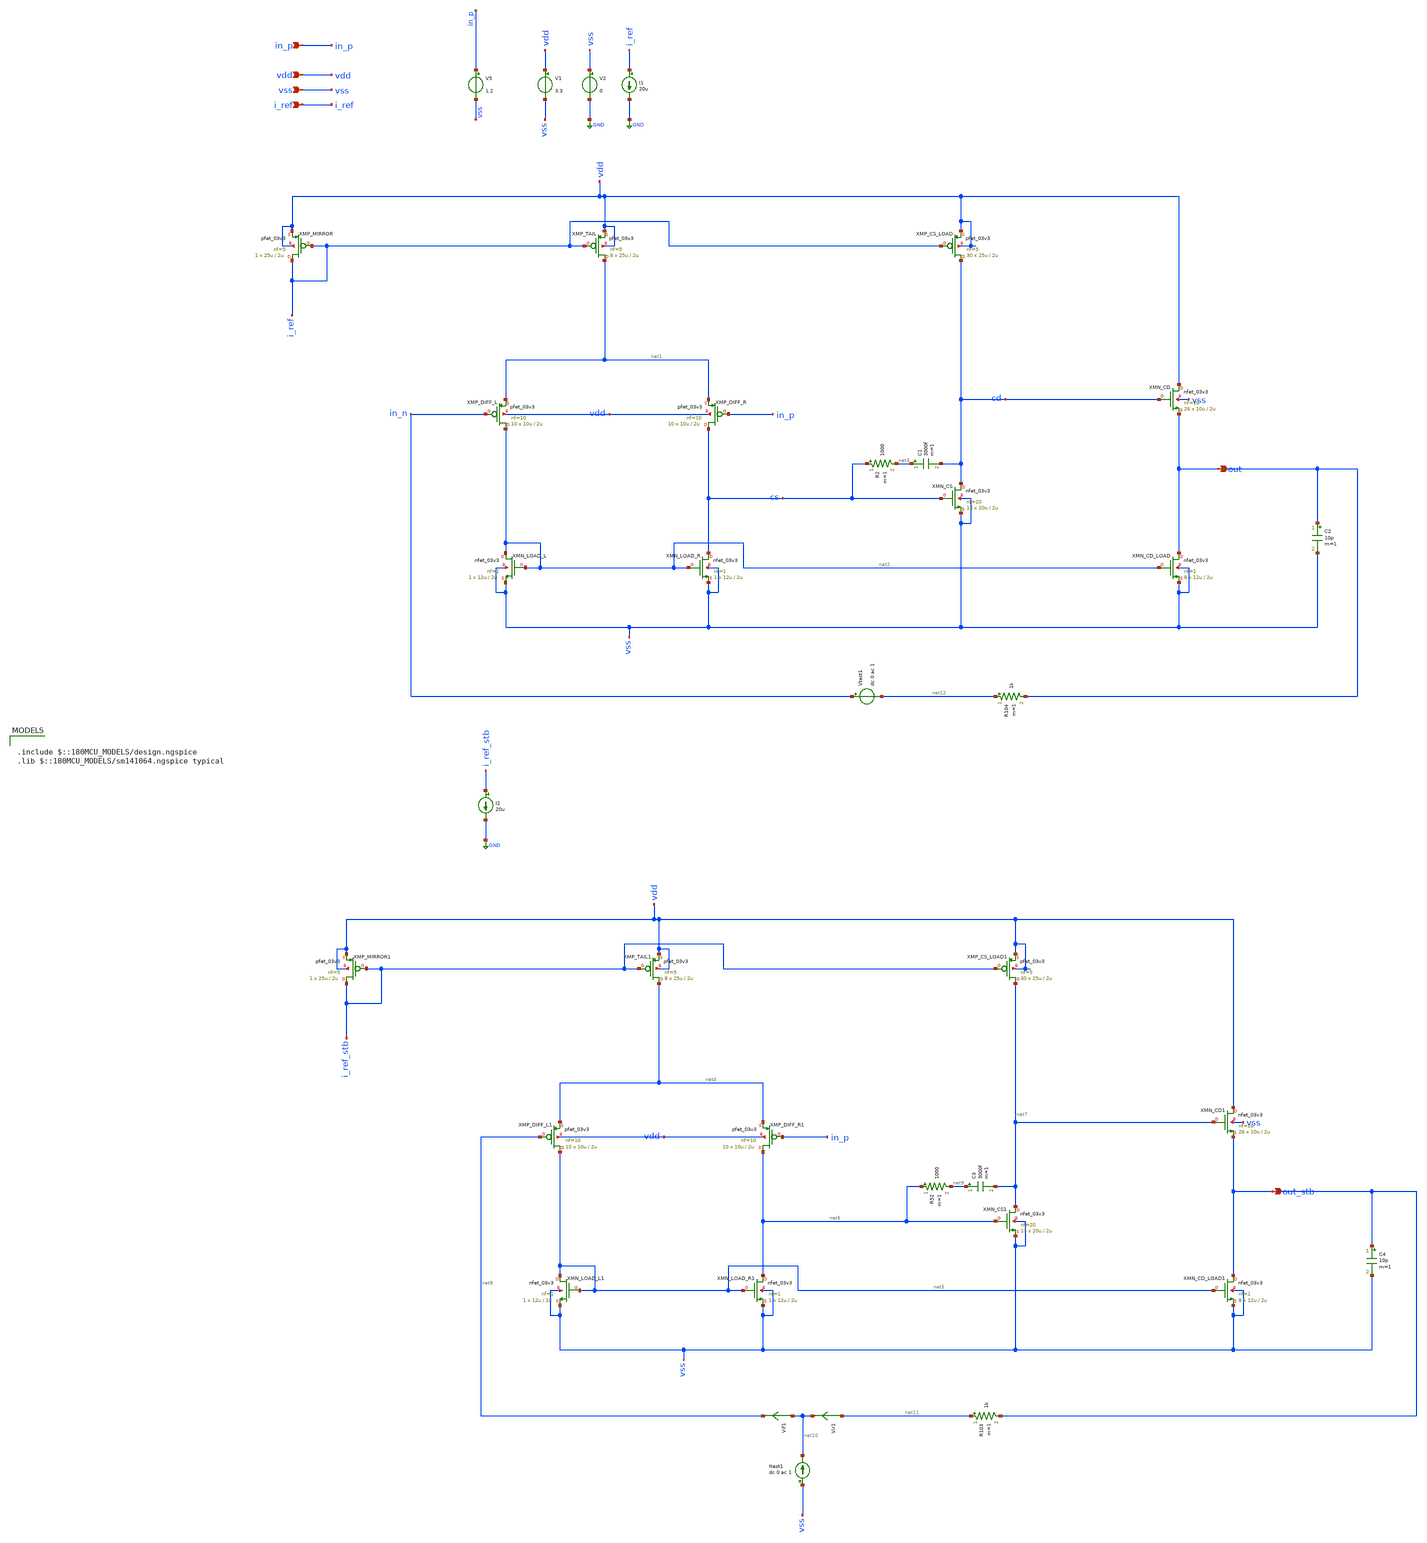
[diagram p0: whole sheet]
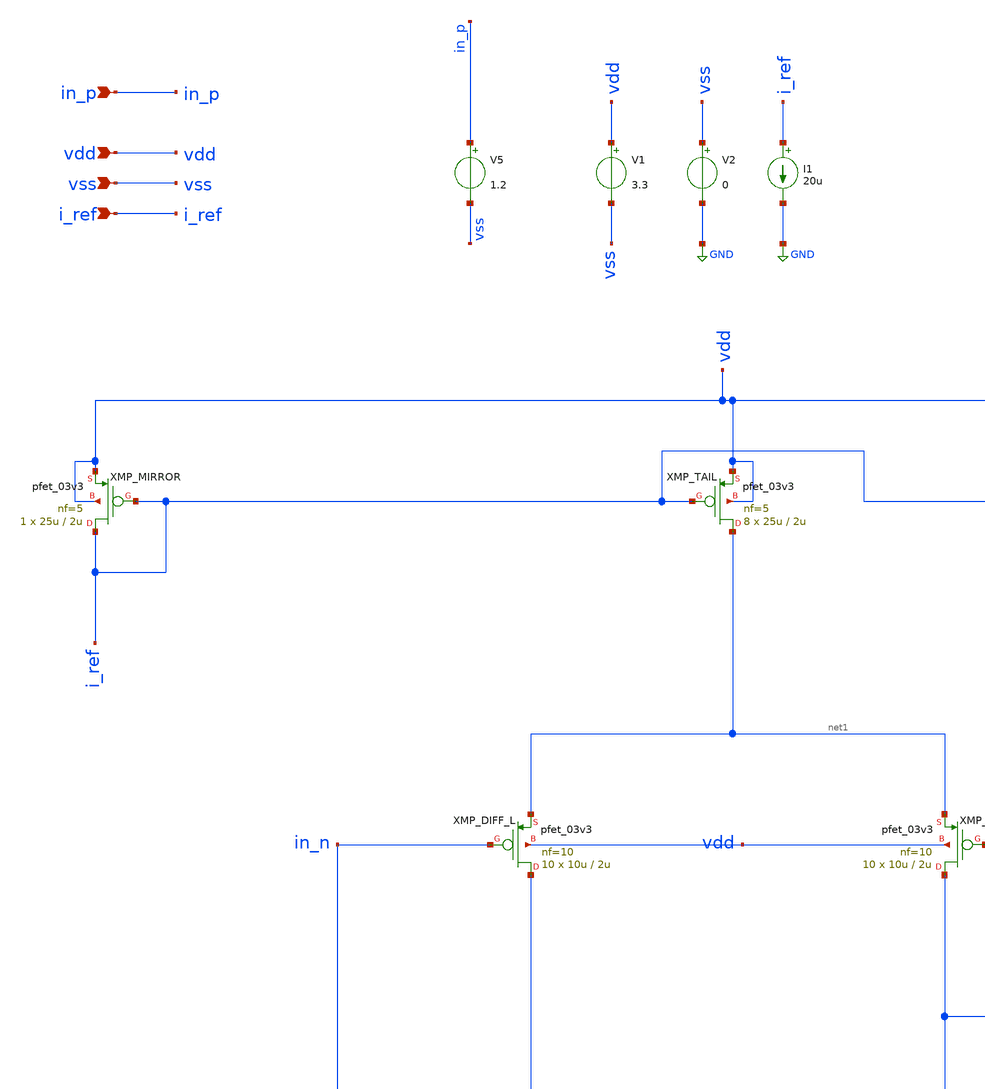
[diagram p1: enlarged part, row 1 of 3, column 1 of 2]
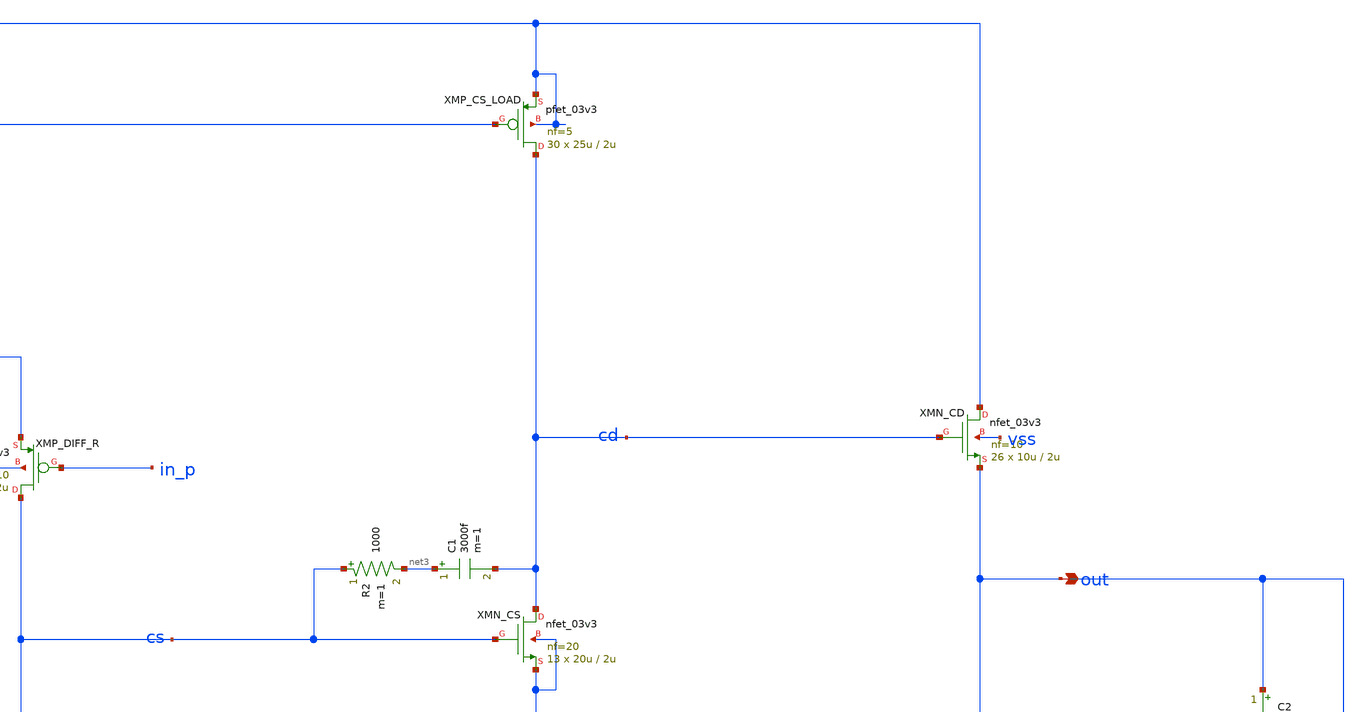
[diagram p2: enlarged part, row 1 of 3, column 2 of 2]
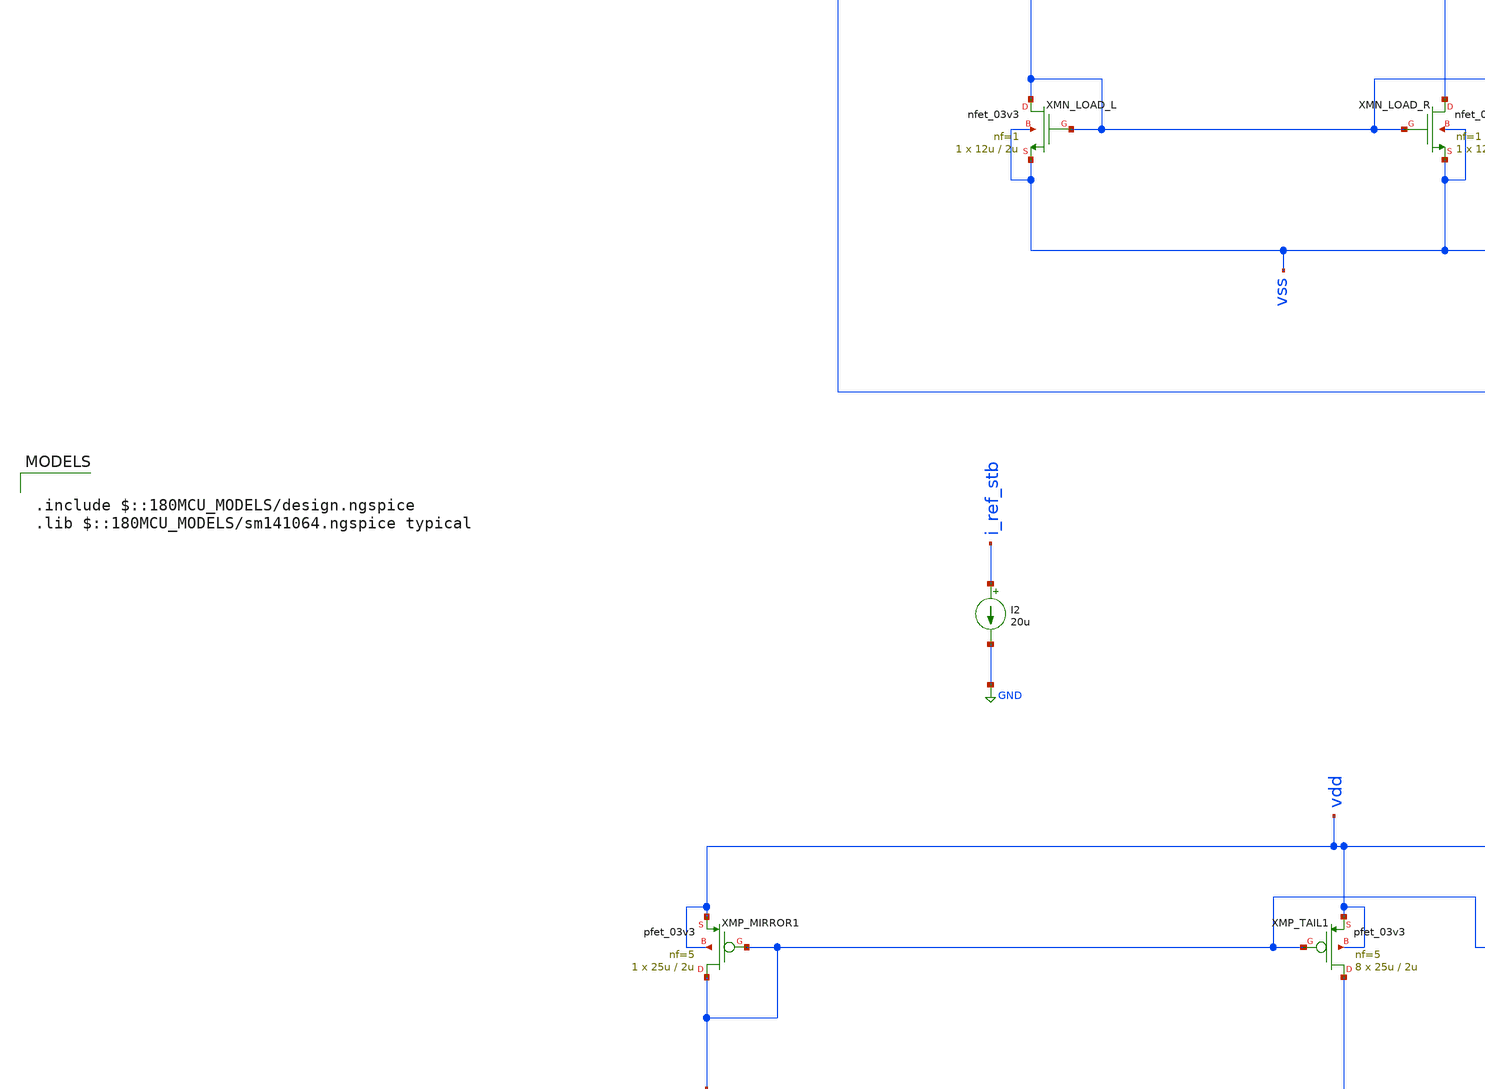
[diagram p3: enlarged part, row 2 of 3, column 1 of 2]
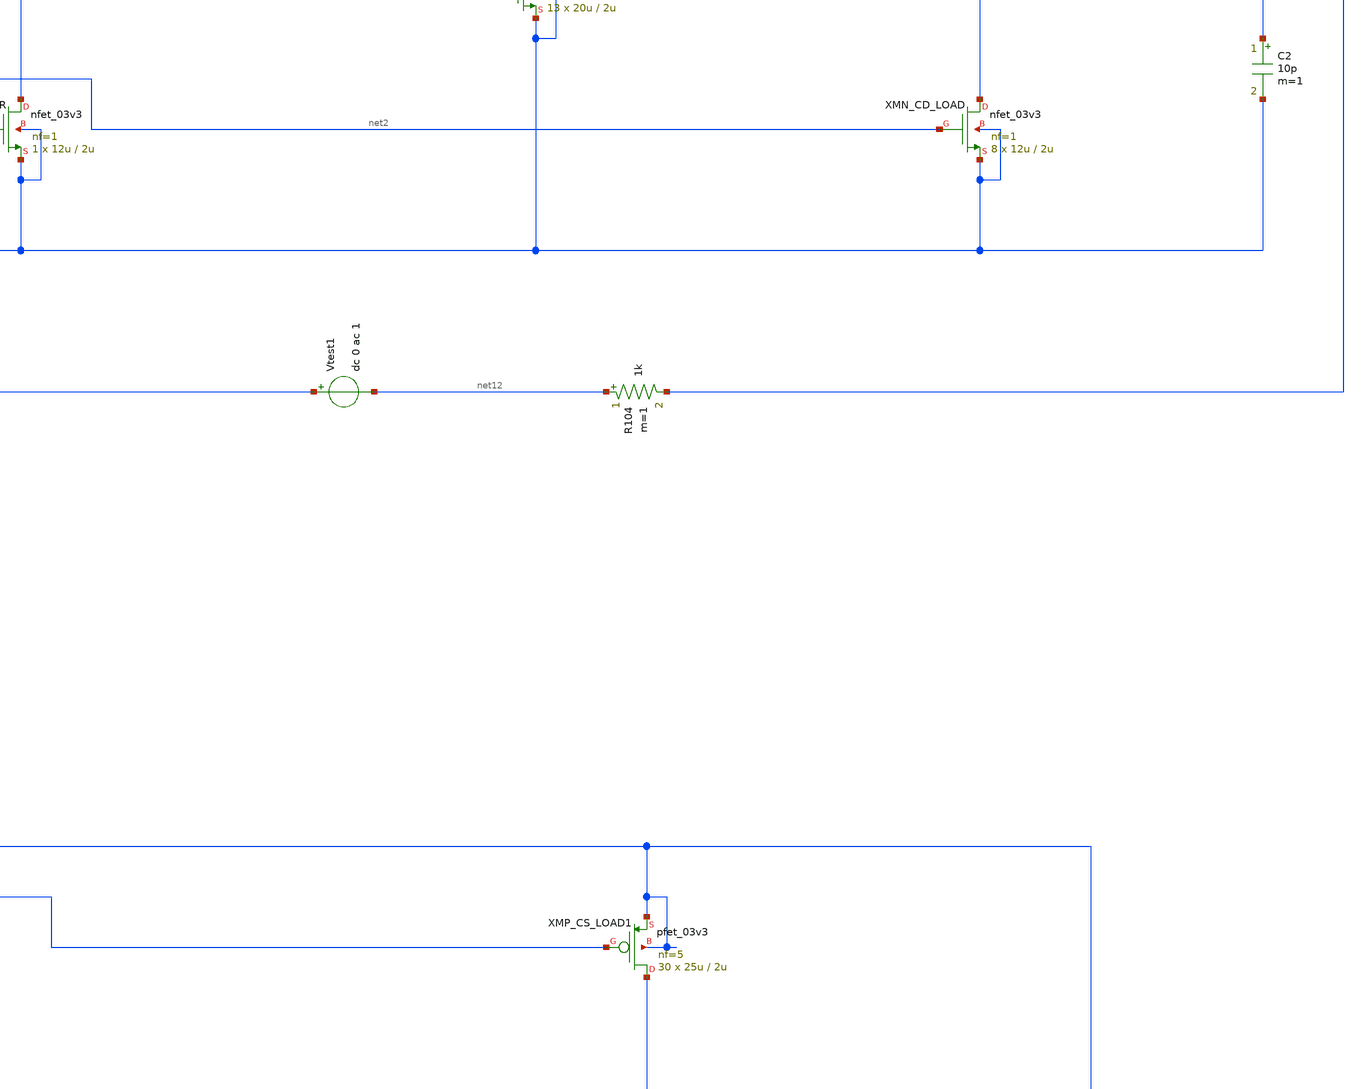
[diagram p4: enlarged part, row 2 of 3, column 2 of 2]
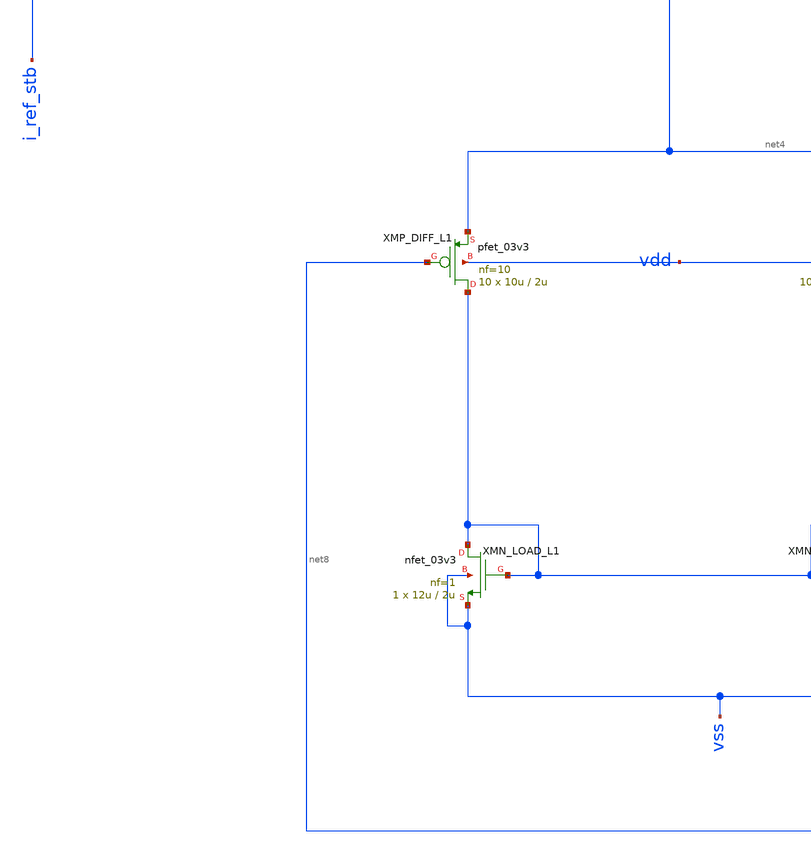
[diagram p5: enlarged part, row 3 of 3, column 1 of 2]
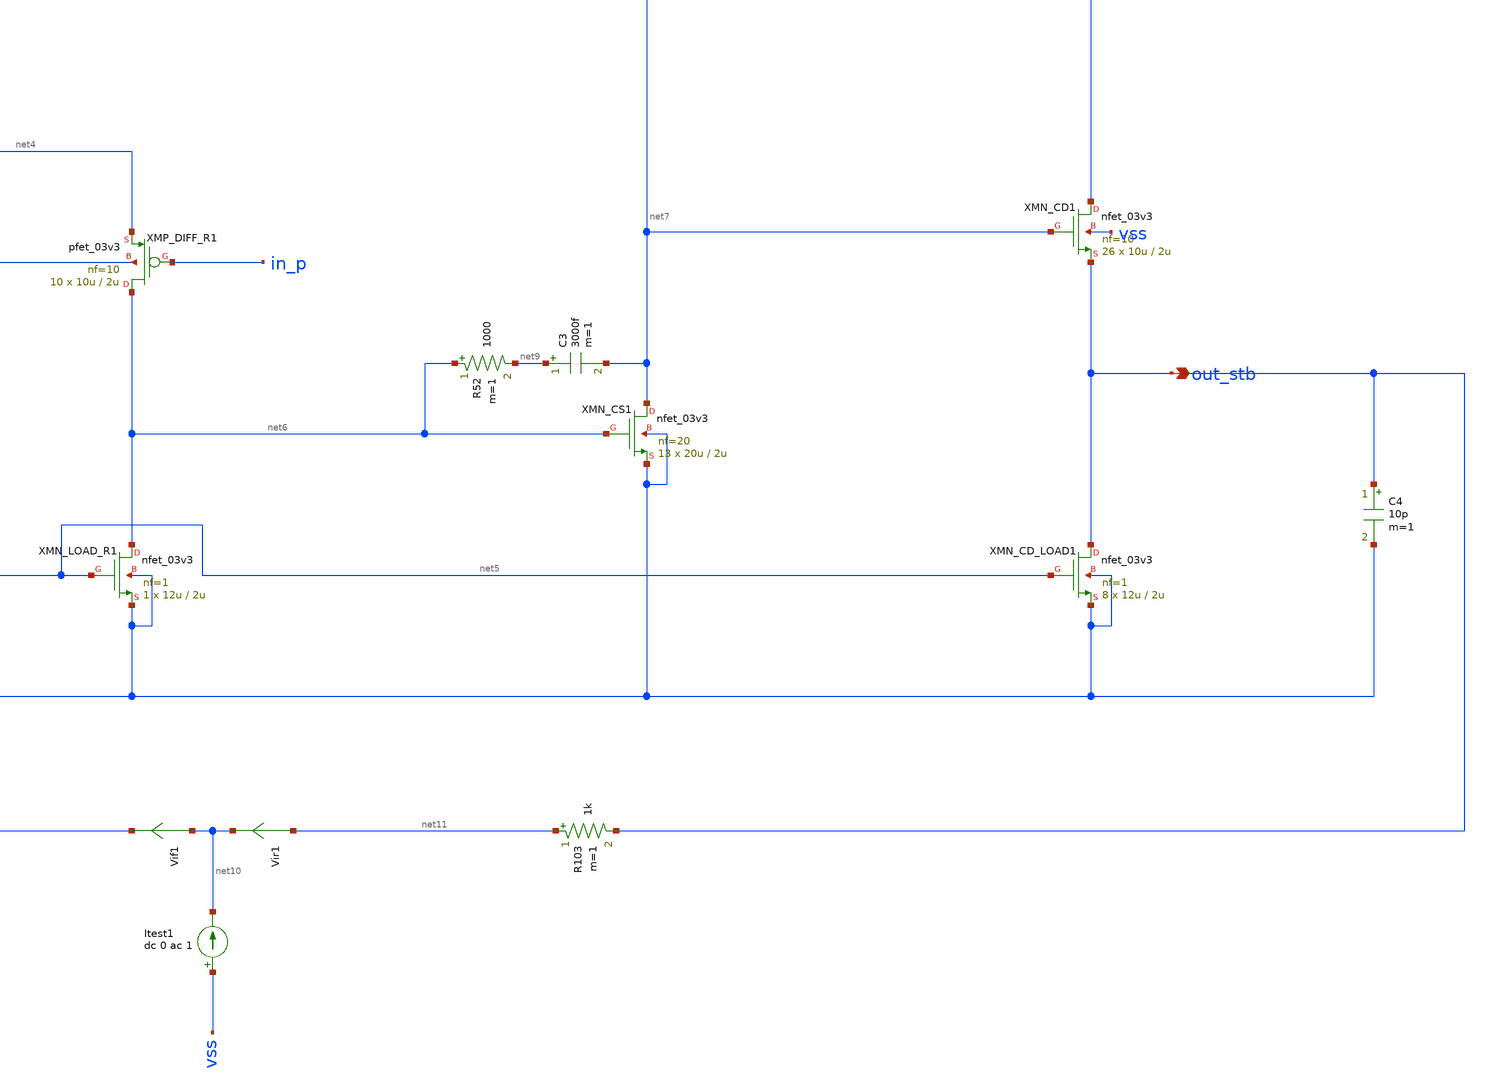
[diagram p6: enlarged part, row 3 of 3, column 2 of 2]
** sch_path: designs/libs/TIA/TIA_TB_stb.sch
**.subckt TIA_TB_stb in_p vdd vss i_ref out out_stb
*.ipin in_p
*.ipin vdd
*.ipin vss
*.ipin i_ref
*.opin out
*.opin out_stb
XMP_TAIL net1 i_ref vdd vdd pfet_03v3 L=2u W=25u nf=5 ad='int((nf+1)/2) * W/nf * 0.18u' as='int((nf+2)/2) * W/nf * 0.18u'
+ pd='2*int((nf+1)/2) * (W/nf + 0.18u)' ps='2*int((nf+2)/2) * (W/nf + 0.18u)' nrd='0.18u / W' nrs='0.18u / W'
+ sa=0 sb=0 sd=0 m=8
XMP_DIFF_L net2 in_n net1 vdd pfet_03v3 L=2u W=10u nf=10 ad='int((nf+1)/2) * W/nf * 0.18u' as='int((nf+2)/2) * W/nf * 0.18u'
+ pd='2*int((nf+1)/2) * (W/nf + 0.18u)' ps='2*int((nf+2)/2) * (W/nf + 0.18u)' nrd='0.18u / W' nrs='0.18u / W'
+ sa=0 sb=0 sd=0 m=10
XMP_DIFF_R cs in_p net1 vdd pfet_03v3 L=2u W=10u nf=10 ad='int((nf+1)/2) * W/nf * 0.18u' as='int((nf+2)/2) * W/nf * 0.18u'
+ pd='2*int((nf+1)/2) * (W/nf + 0.18u)' ps='2*int((nf+2)/2) * (W/nf + 0.18u)' nrd='0.18u / W' nrs='0.18u / W'
+ sa=0 sb=0 sd=0 m=10
XMP_CS_LOAD cd i_ref vdd vdd pfet_03v3 L=2u W=25u nf=5 ad='int((nf+1)/2) * W/nf * 0.18u' as='int((nf+2)/2) * W/nf * 0.18u'
+ pd='2*int((nf+1)/2) * (W/nf + 0.18u)' ps='2*int((nf+2)/2) * (W/nf + 0.18u)' nrd='0.18u / W' nrs='0.18u / W'
+ sa=0 sb=0 sd=0 m=30
XMP_MIRROR i_ref i_ref vdd vdd pfet_03v3 L=2u W=25u nf=5 ad='int((nf+1)/2) * W/nf * 0.18u' as='int((nf+2)/2) * W/nf * 0.18u'
+ pd='2*int((nf+1)/2) * (W/nf + 0.18u)' ps='2*int((nf+2)/2) * (W/nf + 0.18u)' nrd='0.18u / W' nrs='0.18u / W'
+ sa=0 sb=0 sd=0 m=1
XMN_LOAD_R cs net2 vss vss nfet_03v3 L=2u W=12u nf=1 ad='int((nf+1)/2) * W/nf * 0.18u' as='int((nf+2)/2) * W/nf * 0.18u'
+ pd='2*int((nf+1)/2) * (W/nf + 0.18u)' ps='2*int((nf+2)/2) * (W/nf + 0.18u)' nrd='0.18u / W' nrs='0.18u / W'
+ sa=0 sb=0 sd=0 m=1
XMN_LOAD_L net2 net2 vss vss nfet_03v3 L=2u W=12u nf=1 ad='int((nf+1)/2) * W/nf * 0.18u' as='int((nf+2)/2) * W/nf * 0.18u'
+ pd='2*int((nf+1)/2) * (W/nf + 0.18u)' ps='2*int((nf+2)/2) * (W/nf + 0.18u)' nrd='0.18u / W' nrs='0.18u / W'
+ sa=0 sb=0 sd=0 m=1
XMN_CS cd cs vss vss nfet_03v3 L=2u W=20u nf=20 ad='int((nf+1)/2) * W/nf * 0.18u' as='int((nf+2)/2) * W/nf * 0.18u'
+ pd='2*int((nf+1)/2) * (W/nf + 0.18u)' ps='2*int((nf+2)/2) * (W/nf + 0.18u)' nrd='0.18u / W' nrs='0.18u / W'
+ sa=0 sb=0 sd=0 m=13
XMN_CD vdd cd out vss nfet_03v3 L=2u W=10u nf=10 ad='int((nf+1)/2) * W/nf * 0.18u' as='int((nf+2)/2) * W/nf * 0.18u'
+ pd='2*int((nf+1)/2) * (W/nf + 0.18u)' ps='2*int((nf+2)/2) * (W/nf + 0.18u)' nrd='0.18u / W' nrs='0.18u / W'
+ sa=0 sb=0 sd=0 m=26
XMN_CD_LOAD out net2 vss vss nfet_03v3 L=2u W=12u nf=1 ad='int((nf+1)/2) * W/nf * 0.18u' as='int((nf+2)/2) * W/nf * 0.18u'
+ pd='2*int((nf+1)/2) * (W/nf + 0.18u)' ps='2*int((nf+2)/2) * (W/nf + 0.18u)' nrd='0.18u / W' nrs='0.18u / W'
+ sa=0 sb=0 sd=0 m=8
V1 vdd vss 3.3
C1 net3 cd 3000f m=1
R2 cs net3 1000 m=1
V2 vss GND 0
V5 in_p vss 1.2
I1 i_ref GND 20u
C2 out vss 10p m=1
XMP_TAIL1 net4 i_ref_stb vdd vdd pfet_03v3 L=2u W=25u nf=5 ad='int((nf+1)/2) * W/nf * 0.18u' as='int((nf+2)/2) * W/nf * 0.18u'
+ pd='2*int((nf+1)/2) * (W/nf + 0.18u)' ps='2*int((nf+2)/2) * (W/nf + 0.18u)' nrd='0.18u / W' nrs='0.18u / W'
+ sa=0 sb=0 sd=0 m=8
XMP_DIFF_L1 net5 net8 net4 vdd pfet_03v3 L=2u W=10u nf=10 ad='int((nf+1)/2) * W/nf * 0.18u' as='int((nf+2)/2) * W/nf * 0.18u'
+ pd='2*int((nf+1)/2) * (W/nf + 0.18u)' ps='2*int((nf+2)/2) * (W/nf + 0.18u)' nrd='0.18u / W' nrs='0.18u / W'
+ sa=0 sb=0 sd=0 m=10
XMP_DIFF_R1 net6 in_p net4 vdd pfet_03v3 L=2u W=10u nf=10 ad='int((nf+1)/2) * W/nf * 0.18u' as='int((nf+2)/2) * W/nf * 0.18u'
+ pd='2*int((nf+1)/2) * (W/nf + 0.18u)' ps='2*int((nf+2)/2) * (W/nf + 0.18u)' nrd='0.18u / W' nrs='0.18u / W'
+ sa=0 sb=0 sd=0 m=10
XMP_CS_LOAD1 net7 i_ref_stb vdd vdd pfet_03v3 L=2u W=25u nf=5 ad='int((nf+1)/2) * W/nf * 0.18u' as='int((nf+2)/2) * W/nf * 0.18u'
+ pd='2*int((nf+1)/2) * (W/nf + 0.18u)' ps='2*int((nf+2)/2) * (W/nf + 0.18u)' nrd='0.18u / W' nrs='0.18u / W'
+ sa=0 sb=0 sd=0 m=30
XMP_MIRROR1 i_ref_stb i_ref_stb vdd vdd pfet_03v3 L=2u W=25u nf=5 ad='int((nf+1)/2) * W/nf * 0.18u' as='int((nf+2)/2) * W/nf * 0.18u'
+ pd='2*int((nf+1)/2) * (W/nf + 0.18u)' ps='2*int((nf+2)/2) * (W/nf + 0.18u)' nrd='0.18u / W' nrs='0.18u / W'
+ sa=0 sb=0 sd=0 m=1
XMN_LOAD_R1 net6 net5 vss vss nfet_03v3 L=2u W=12u nf=1 ad='int((nf+1)/2) * W/nf * 0.18u' as='int((nf+2)/2) * W/nf * 0.18u'
+ pd='2*int((nf+1)/2) * (W/nf + 0.18u)' ps='2*int((nf+2)/2) * (W/nf + 0.18u)' nrd='0.18u / W' nrs='0.18u / W'
+ sa=0 sb=0 sd=0 m=1
XMN_LOAD_L1 net5 net5 vss vss nfet_03v3 L=2u W=12u nf=1 ad='int((nf+1)/2) * W/nf * 0.18u' as='int((nf+2)/2) * W/nf * 0.18u'
+ pd='2*int((nf+1)/2) * (W/nf + 0.18u)' ps='2*int((nf+2)/2) * (W/nf + 0.18u)' nrd='0.18u / W' nrs='0.18u / W'
+ sa=0 sb=0 sd=0 m=1
XMN_CS1 net7 net6 vss vss nfet_03v3 L=2u W=20u nf=20 ad='int((nf+1)/2) * W/nf * 0.18u' as='int((nf+2)/2) * W/nf * 0.18u'
+ pd='2*int((nf+1)/2) * (W/nf + 0.18u)' ps='2*int((nf+2)/2) * (W/nf + 0.18u)' nrd='0.18u / W' nrs='0.18u / W'
+ sa=0 sb=0 sd=0 m=13
XMN_CD1 vdd net7 out_stb vss nfet_03v3 L=2u W=10u nf=10 ad='int((nf+1)/2) * W/nf * 0.18u' as='int((nf+2)/2) * W/nf * 0.18u'
+ pd='2*int((nf+1)/2) * (W/nf + 0.18u)' ps='2*int((nf+2)/2) * (W/nf + 0.18u)' nrd='0.18u / W' nrs='0.18u / W'
+ sa=0 sb=0 sd=0 m=26
XMN_CD_LOAD1 out_stb net5 vss vss nfet_03v3 L=2u W=12u nf=1 ad='int((nf+1)/2) * W/nf * 0.18u' as='int((nf+2)/2) * W/nf * 0.18u'
+ pd='2*int((nf+1)/2) * (W/nf + 0.18u)' ps='2*int((nf+2)/2) * (W/nf + 0.18u)' nrd='0.18u / W' nrs='0.18u / W'
+ sa=0 sb=0 sd=0 m=8
C3 net9 net7 3000f m=1
R52 net6 net9 1000 m=1
C4 out_stb vss 10p m=1
I2 i_ref_stb GND 20u
Vtest1 in_n net12 dc 0 ac 1
Vir1 net11 net10 0
.save i(vir1)
Vif1 net10 net8 0
.save i(vif1)
Itest1 vss net10 dc 0 ac 1
R103 net11 out_stb 1k m=1
R104 net12 out 1k m=1
**** begin user architecture code


.save @m.xmp_mirror.m0[gds]
.save @m.xmp_mirror.m0[gm]
.save @m.xmp_mirror.m0[id]
.save @m.xmp_mirror.m0[vth]
.save @m.xmp_mirror.m0[vdsat]
.save @m.xmp_mirror.m0[vds]


.save @m.xmp_tail.m0[gds]
.save @m.xmp_tail.m0[gm]
.save @m.xmp_tail.m0[id]
.save @m.xmp_tail.m0[vth]
.save @m.xmp_tail.m0[vdsat]
.save @m.xmp_tail.m0[vds]

.save @m.xmp_diff_l.m0[gds]
.save @m.xmp_diff_l.m0[gm]
.save @m.xmp_diff_l.m0[id]
.save @m.xmp_diff_l.m0[vth]
.save @m.xmp_diff_l.m0[vdsat]
.save @m.xmp_diff_l.m0[vds]

.save @m.xmp_diff_r.m0[gds]
.save @m.xmp_diff_r.m0[gm]
.save @m.xmp_diff_r.m0[id]
.save @m.xmp_diff_r.m0[vth]
.save @m.xmp_diff_r.m0[vdsat]
.save @m.xmp_diff_r.m0[vds]

.save @m.xmn_load_l.m0[gds]
.save @m.xmn_load_l.m0[gm]
.save @m.xmn_load_l.m0[id]
.save @m.xmn_load_l.m0[vth]
.save @m.xmn_load_l.m0[vdsat]
.save @m.xmn_load_l.m0[vds]

.save @m.xmn_load_r.m0[gds]
.save @m.xmn_load_r.m0[gm]
.save @m.xmn_load_r.m0[id]
.save @m.xmn_load_r.m0[vth]
.save @m.xmn_load_r.m0[vdsat]
.save @m.xmn_load_r.m0[vds]

.save @m.xmp_cs_load.m0[gds]
.save @m.xmp_cs_load.m0[gm]
.save @m.xmp_cs_load.m0[id]
.save @m.xmp_cs_load.m0[vth]
.save @m.xmp_cs_load.m0[vdsat]
.save @m.xmp_cs_load.m0[vds]

.save @m.xmn_cs.m0[gds]
.save @m.xmn_cs.m0[gm]
.save @m.xmn_cs.m0[id]
.save @m.xmn_cs.m0[vth]
.save @m.xmn_cs.m0[vdsat]
.save @m.xmn_cs.m0[vds]

.save @m.xmn_cd_load.m0[gds]
.save @m.xmn_cd_load.m0[gm]
.save @m.xmn_cd_load.m0[id]
.save @m.xmn_cd_load.m0[vth]
.save @m.xmn_cd_load.m0[vdsat]
.save @m.xmn_cd_load.m0[vds]

.save @m.xmn_cd.m0[gds]
.save @m.xmn_cd.m0[gm]
.save @m.xmn_cd.m0[id]
.save @m.xmn_cd.m0[vth]
.save @m.xmn_cd.m0[vdsat]
.save @m.xmn_cd.m0[vds]







.control
save all


** Simulation
op
ac dec 1001 1 1G
**remzerovec
write TIA_TB_stb.raw
**set appendwrite

* Middlebrook's Method
let tv=-v(out)/v(in_n)
let ti=-i(vir1)/i(vif1)
let tmb=(tv*ti - 1)/(tv + ti + 2)

plot db(tmb) ylabel 'Magnitude - Middlebrook'
plot 180/pi*cphase(tmb) ylabel 'Phase - Middlebrook'

setplot op1
print @m.xmp_mirror.m0[id]
print cs
print cd
print out

print @m.xmn_cs.m0[vdsat]
print @m.xmn_cs.m0[vds]

print @m.xmp_cs_load.m0[vdsat]
print @m.xmp_cs_load.m0[vds]

print @m.xmn_cd.m0[vdsat]
print @m.xmn_cd.m0[vds]

print @m.xmn_cd_load.m0[vdsat]
print @m.xmn_cd_load.m0[vds]

** Plots

**setplot new
**set curplottitle=Loopgain
**let frequency = ac1.frequency
**let T = (ac1.i(V6) + ac2.i(V4))/(ac1.i(V4) + ac2.i(V6))
**let Tmag = db(T)
**let Tphase = 180*cph(T)/pi
**plot Tmag Tphase xlog


.endc



.include $::180MCU_MODELS/design.ngspice
.lib $::180MCU_MODELS/sm141064.ngspice typical

**** end user architecture code
**.ends
.GLOBAL GND
.end
